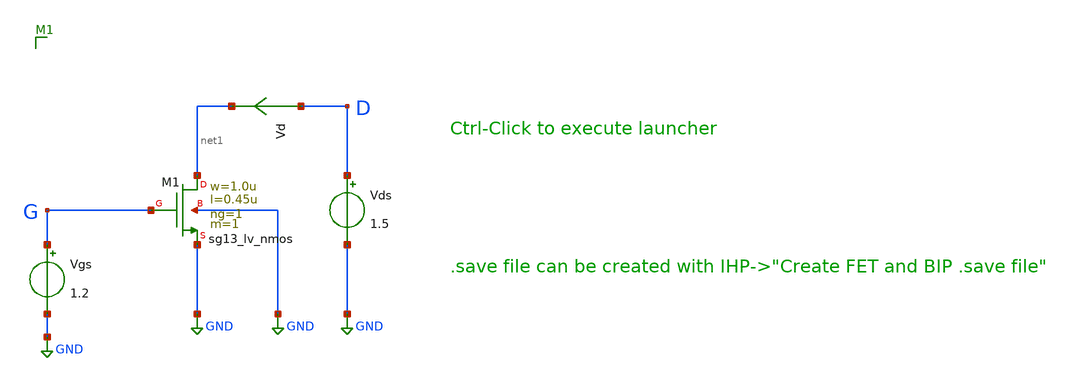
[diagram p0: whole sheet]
** sch_path: ihp-sg13g2/xschem_libs/sg13g2_tests_ase/dc_lv_nmos/schematic/dc_lv_nmos.sch
* Copyright 2023 IHP PDK Authors
**.subckt dc_lv_nmos
Vgs G GND 1.2
Vds D GND 1.5
Vd D net1 0
.save i(vd)
XM1 net1 G GND GND sg13_lv_nmos w=1.0u l=0.45u ng=1 m=1 mm_ok=1
**.ends
.GLOBAL GND
.end
